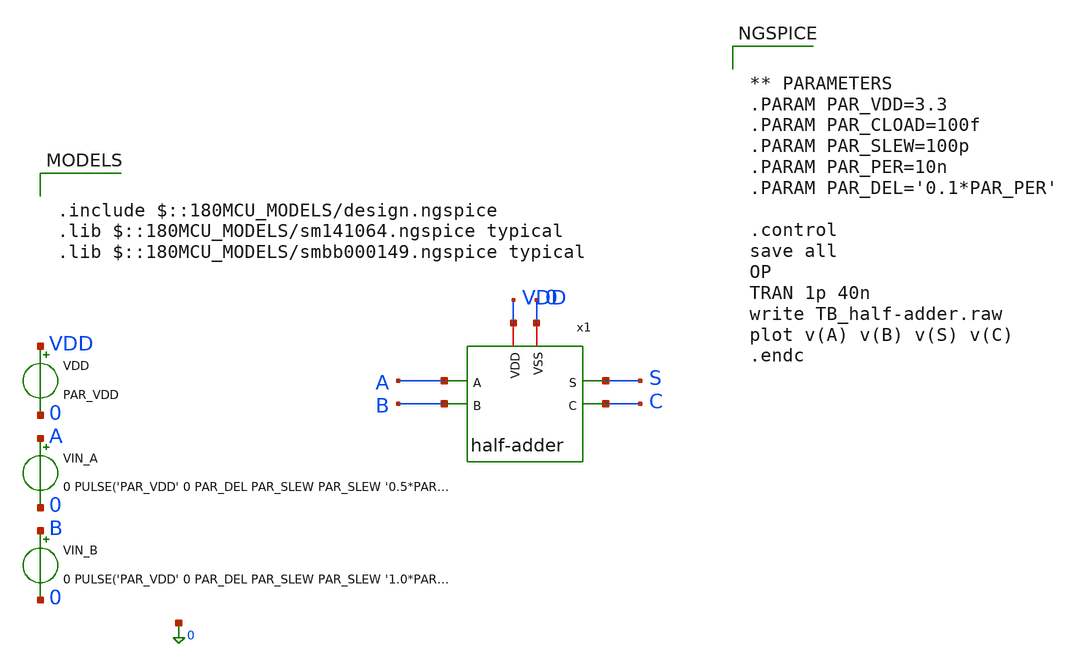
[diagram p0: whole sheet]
** sch_path: schematics/components/half-adder/half-adder_tb.sch
**.subckt half-adder_tb
VIN_A A 0 0 PULSE('PAR_VDD' 0 PAR_DEL PAR_SLEW PAR_SLEW '0.5*PAR_PER' '1.0*PAR_PER')
VDD VDD 0 PAR_VDD
x1 A B S C VDD 0 half-adder
VIN_B B 0 0 PULSE('PAR_VDD' 0 PAR_DEL PAR_SLEW PAR_SLEW '1.0*PAR_PER' '2.0*PAR_PER')
**** begin user architecture code

.include $::180MCU_MODELS/design.ngspice
.lib $::180MCU_MODELS/sm141064.ngspice typical
.lib $::180MCU_MODELS/smbb000149.ngspice typical



** PARAMETERS
.PARAM PAR_VDD=3.3
.PARAM PAR_CLOAD=100f
.PARAM PAR_SLEW=100p
.PARAM PAR_PER=10n
.PARAM PAR_DEL='0.1*PAR_PER'

.control
save all
OP
TRAN 1p 40n
write TB_half-adder.raw
plot v(A) v(B) v(S) v(C)
.endc



**** end user architecture code
**.ends

* expanding   symbol:  schematics/components/half-adder/half-adder.sym # of pins=6
** sym_path: schematics/components/half-adder/half-adder.sym
** sch_path: schematics/components/half-adder/half-adder.sch
.subckt half-adder A B S C VDD VSS
*.ipin A
*.ipin B
*.opin S
*.opin C
*.iopin VDD
*.iopin VSS
x1 A B net1 S VDD VSS xor
x2 A B net2 C VDD VSS and
.ends


* expanding   symbol:  schematics/logic-gates/xor/xor.sym # of pins=6
** sym_path: schematics/logic-gates/xor/xor.sym
** sch_path: schematics/logic-gates/xor/xor.sch
.subckt xor A B N_C C VDD VSS
*.ipin A
*.ipin B
*.opin C
*.opin N_C
*.iopin VDD
*.iopin VSS
XM1 N_A A VSS VSS nfet_03v3 L=0.28u W=0.22u nf=1 ad='int((nf+1)/2) * W/nf * 0.18u' as='int((nf+2)/2) * W/nf * 0.18u'
+ pd='2*int((nf+1)/2) * (W/nf + 0.18u)' ps='2*int((nf+2)/2) * (W/nf + 0.18u)' nrd='0.18u / W' nrs='0.18u / W'
+ sa=0 sb=0 sd=0 m=1
XM2 N_A A VDD VDD pfet_03v3 L=0.28u W=0.22u nf=1 ad='int((nf+1)/2) * W/nf * 0.18u' as='int((nf+2)/2) * W/nf * 0.18u'
+ pd='2*int((nf+1)/2) * (W/nf + 0.18u)' ps='2*int((nf+2)/2) * (W/nf + 0.18u)' nrd='0.18u / W' nrs='0.18u / W'
+ sa=0 sb=0 sd=0 m=1
XM3 N_B B VDD VDD pfet_03v3 L=0.28u W=0.22u nf=1 ad='int((nf+1)/2) * W/nf * 0.18u' as='int((nf+2)/2) * W/nf * 0.18u'
+ pd='2*int((nf+1)/2) * (W/nf + 0.18u)' ps='2*int((nf+2)/2) * (W/nf + 0.18u)' nrd='0.18u / W' nrs='0.18u / W'
+ sa=0 sb=0 sd=0 m=1
XM4 N_B B VSS VSS nfet_03v3 L=0.28u W=0.22u nf=1 ad='int((nf+1)/2) * W/nf * 0.18u' as='int((nf+2)/2) * W/nf * 0.18u'
+ pd='2*int((nf+1)/2) * (W/nf + 0.18u)' ps='2*int((nf+2)/2) * (W/nf + 0.18u)' nrd='0.18u / W' nrs='0.18u / W'
+ sa=0 sb=0 sd=0 m=1
XM5 net2 B VSS VSS nfet_03v3 L=0.28u W=0.22u nf=1 ad='int((nf+1)/2) * W/nf * 0.18u' as='int((nf+2)/2) * W/nf * 0.18u'
+ pd='2*int((nf+1)/2) * (W/nf + 0.18u)' ps='2*int((nf+2)/2) * (W/nf + 0.18u)' nrd='0.18u / W' nrs='0.18u / W'
+ sa=0 sb=0 sd=0 m=1
XM6 net3 N_B VSS VSS nfet_03v3 L=0.28u W=0.22u nf=1 ad='int((nf+1)/2) * W/nf * 0.18u' as='int((nf+2)/2) * W/nf * 0.18u'
+ pd='2*int((nf+1)/2) * (W/nf + 0.18u)' ps='2*int((nf+2)/2) * (W/nf + 0.18u)' nrd='0.18u / W' nrs='0.18u / W'
+ sa=0 sb=0 sd=0 m=1
XM7 C A net2 VSS nfet_03v3 L=0.28u W=0.22u nf=1 ad='int((nf+1)/2) * W/nf * 0.18u' as='int((nf+2)/2) * W/nf * 0.18u'
+ pd='2*int((nf+1)/2) * (W/nf + 0.18u)' ps='2*int((nf+2)/2) * (W/nf + 0.18u)' nrd='0.18u / W' nrs='0.18u / W'
+ sa=0 sb=0 sd=0 m=1
XM8 C N_A net3 VSS nfet_03v3 L=0.28u W=0.22u nf=1 ad='int((nf+1)/2) * W/nf * 0.18u' as='int((nf+2)/2) * W/nf * 0.18u'
+ pd='2*int((nf+1)/2) * (W/nf + 0.18u)' ps='2*int((nf+2)/2) * (W/nf + 0.18u)' nrd='0.18u / W' nrs='0.18u / W'
+ sa=0 sb=0 sd=0 m=1
XM9 C B net1 VDD pfet_03v3 L=0.28u W=0.22u nf=1 ad='int((nf+1)/2) * W/nf * 0.18u' as='int((nf+2)/2) * W/nf * 0.18u'
+ pd='2*int((nf+1)/2) * (W/nf + 0.18u)' ps='2*int((nf+2)/2) * (W/nf + 0.18u)' nrd='0.18u / W' nrs='0.18u / W'
+ sa=0 sb=0 sd=0 m=1
XM10 C N_B net4 VDD pfet_03v3 L=0.28u W=0.22u nf=1 ad='int((nf+1)/2) * W/nf * 0.18u' as='int((nf+2)/2) * W/nf * 0.18u'
+ pd='2*int((nf+1)/2) * (W/nf + 0.18u)' ps='2*int((nf+2)/2) * (W/nf + 0.18u)' nrd='0.18u / W' nrs='0.18u / W'
+ sa=0 sb=0 sd=0 m=1
XM11 net1 N_A VDD VDD pfet_03v3 L=0.28u W=0.22u nf=1 ad='int((nf+1)/2) * W/nf * 0.18u' as='int((nf+2)/2) * W/nf * 0.18u'
+ pd='2*int((nf+1)/2) * (W/nf + 0.18u)' ps='2*int((nf+2)/2) * (W/nf + 0.18u)' nrd='0.18u / W' nrs='0.18u / W'
+ sa=0 sb=0 sd=0 m=1
XM12 net4 A VDD VDD pfet_03v3 L=0.28u W=0.22u nf=1 ad='int((nf+1)/2) * W/nf * 0.18u' as='int((nf+2)/2) * W/nf * 0.18u'
+ pd='2*int((nf+1)/2) * (W/nf + 0.18u)' ps='2*int((nf+2)/2) * (W/nf + 0.18u)' nrd='0.18u / W' nrs='0.18u / W'
+ sa=0 sb=0 sd=0 m=1
XM13 N_C C VDD VDD pfet_03v3 L=0.28u W=0.22u nf=1 ad='int((nf+1)/2) * W/nf * 0.18u' as='int((nf+2)/2) * W/nf * 0.18u'
+ pd='2*int((nf+1)/2) * (W/nf + 0.18u)' ps='2*int((nf+2)/2) * (W/nf + 0.18u)' nrd='0.18u / W' nrs='0.18u / W'
+ sa=0 sb=0 sd=0 m=1
XM14 N_C C VSS VSS nfet_03v3 L=0.28u W=0.22u nf=1 ad='int((nf+1)/2) * W/nf * 0.18u' as='int((nf+2)/2) * W/nf * 0.18u'
+ pd='2*int((nf+1)/2) * (W/nf + 0.18u)' ps='2*int((nf+2)/2) * (W/nf + 0.18u)' nrd='0.18u / W' nrs='0.18u / W'
+ sa=0 sb=0 sd=0 m=1
.ends


* expanding   symbol:  schematics/logic-gates/and/and.sym # of pins=6
** sym_path: schematics/logic-gates/and/and.sym
** sch_path: schematics/logic-gates/and/and.sch
.subckt and A B N_C C VDD VSS
*.ipin A
*.ipin B
*.opin C
*.opin N_C
*.iopin VDD
*.iopin VSS
XM1 N_C B net1 VSS nfet_03v3 L=0.28u W=0.22u nf=1 ad='int((nf+1)/2) * W/nf * 0.18u' as='int((nf+2)/2) * W/nf * 0.18u'
+ pd='2*int((nf+1)/2) * (W/nf + 0.18u)' ps='2*int((nf+2)/2) * (W/nf + 0.18u)' nrd='0.18u / W' nrs='0.18u / W'
+ sa=0 sb=0 sd=0 m=1
XM2 N_C A VDD VDD pfet_03v3 L=0.28u W=0.22u nf=1 ad='int((nf+1)/2) * W/nf * 0.18u' as='int((nf+2)/2) * W/nf * 0.18u'
+ pd='2*int((nf+1)/2) * (W/nf + 0.18u)' ps='2*int((nf+2)/2) * (W/nf + 0.18u)' nrd='0.18u / W' nrs='0.18u / W'
+ sa=0 sb=0 sd=0 m=1
XM3 N_C B VDD VDD pfet_03v3 L=0.28u W=0.22u nf=1 ad='int((nf+1)/2) * W/nf * 0.18u' as='int((nf+2)/2) * W/nf * 0.18u'
+ pd='2*int((nf+1)/2) * (W/nf + 0.18u)' ps='2*int((nf+2)/2) * (W/nf + 0.18u)' nrd='0.18u / W' nrs='0.18u / W'
+ sa=0 sb=0 sd=0 m=1
XM4 net1 A VSS VSS nfet_03v3 L=0.28u W=0.22u nf=1 ad='int((nf+1)/2) * W/nf * 0.18u' as='int((nf+2)/2) * W/nf * 0.18u'
+ pd='2*int((nf+1)/2) * (W/nf + 0.18u)' ps='2*int((nf+2)/2) * (W/nf + 0.18u)' nrd='0.18u / W' nrs='0.18u / W'
+ sa=0 sb=0 sd=0 m=1
XM5 C N_C VDD VDD pfet_03v3 L=0.28u W=0.22u nf=1 ad='int((nf+1)/2) * W/nf * 0.18u' as='int((nf+2)/2) * W/nf * 0.18u'
+ pd='2*int((nf+1)/2) * (W/nf + 0.18u)' ps='2*int((nf+2)/2) * (W/nf + 0.18u)' nrd='0.18u / W' nrs='0.18u / W'
+ sa=0 sb=0 sd=0 m=1
XM6 C N_C VSS VSS nfet_03v3 L=0.28u W=0.22u nf=1 ad='int((nf+1)/2) * W/nf * 0.18u' as='int((nf+2)/2) * W/nf * 0.18u'
+ pd='2*int((nf+1)/2) * (W/nf + 0.18u)' ps='2*int((nf+2)/2) * (W/nf + 0.18u)' nrd='0.18u / W' nrs='0.18u / W'
+ sa=0 sb=0 sd=0 m=1
.ends

.end
